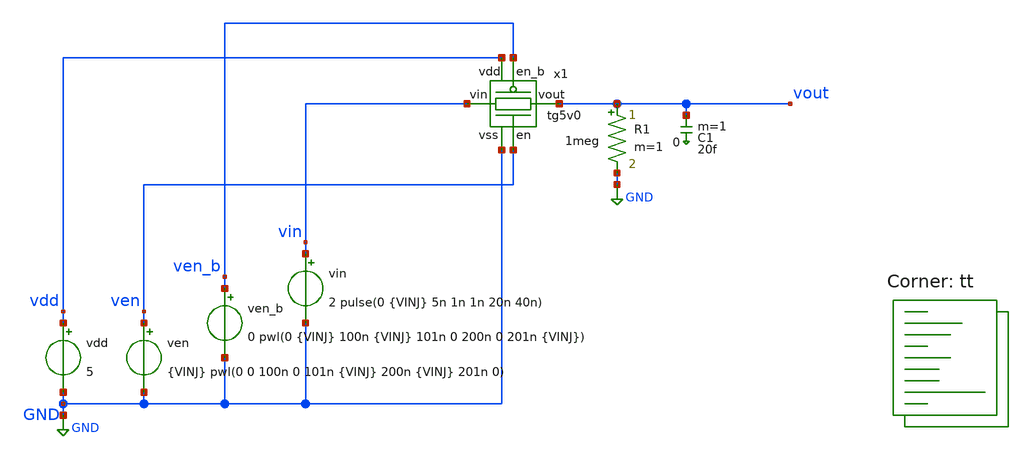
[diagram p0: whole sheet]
** sch_path: xschem/test_tg5v0.sch
**.subckt test_tg5v0
x1 vin vout ven ven_b vdd GND tg5v0
ven ven GND {VINJ} pwl(0 0 100n 0 101n {VINJ} 200n {VINJ} 201n 0)
vin vin GND 2 pulse(0 {VINJ} 5n 1n 1n 20n 40n)
ven_b ven_b GND 0 pwl(0 {VINJ} 100n {VINJ} 101n 0 200n 0 201n {VINJ})
vdd vdd GND 5
R1 vout GND 1meg m=1
C1 vout 0 20f m=1
**** begin user architecture code
.lib $::SKYWATER_MODELS/sky130.lib.spice tt



.include 'tg5v0.spice'
* .options reltol=0.0001 abstol=10e-15
.param VINJ=5
.param VSS=0
.options savecurrents
.control
  save all
  op
  remzerovec
  write test_tg5v0.raw
  set appendwrite
  * dc sweep
  dc vin 0 5 0.1
  remzerovec
  write test_tg5v0.raw
  * tran
  tran 100p 300n
  remzerovec
  write test_tg5v0.raw
.endc



**** end user architecture code
**.ends
.GLOBAL GND
.end
